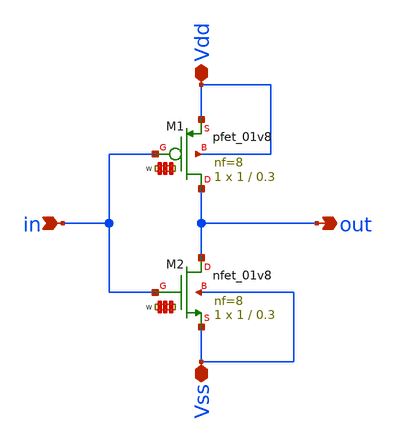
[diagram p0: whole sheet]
** sch_path: Circuits/Buffer/inverter.sch
**.subckt inverter Vdd Vss in out
*.iopin Vdd
*.iopin Vss
*.ipin in
*.opin out
XM1 out in Vdd Vdd sky130_fd_pr__pfet_01v8 L=0.3 W='1 * 8 ' nf=8 ad='int((nf+1)/2) * W / nf * 0.29' as='int((nf+2)/2) * W / nf * 0.29'
+ pd='2*int((nf+1)/2) * (W / nf + 0.29)' ps='2*int((nf+2)/2) * (W / nf + 0.29)' nrd='0.29 / W ' nrs='0.29 / W '
+ sa=0 sb=0 sd=0 mult=1 m=1
XM2 out in Vss Vss sky130_fd_pr__nfet_01v8 L=0.3 W='1 * 8 ' nf=8 ad='int((nf+1)/2) * W / nf * 0.29' as='int((nf+2)/2) * W / nf * 0.29'
+ pd='2*int((nf+1)/2) * (W / nf + 0.29)' ps='2*int((nf+2)/2) * (W / nf + 0.29)' nrd='0.29 / W ' nrs='0.29 / W '
+ sa=0 sb=0 sd=0 mult=1 m=1
**.ends
.end
